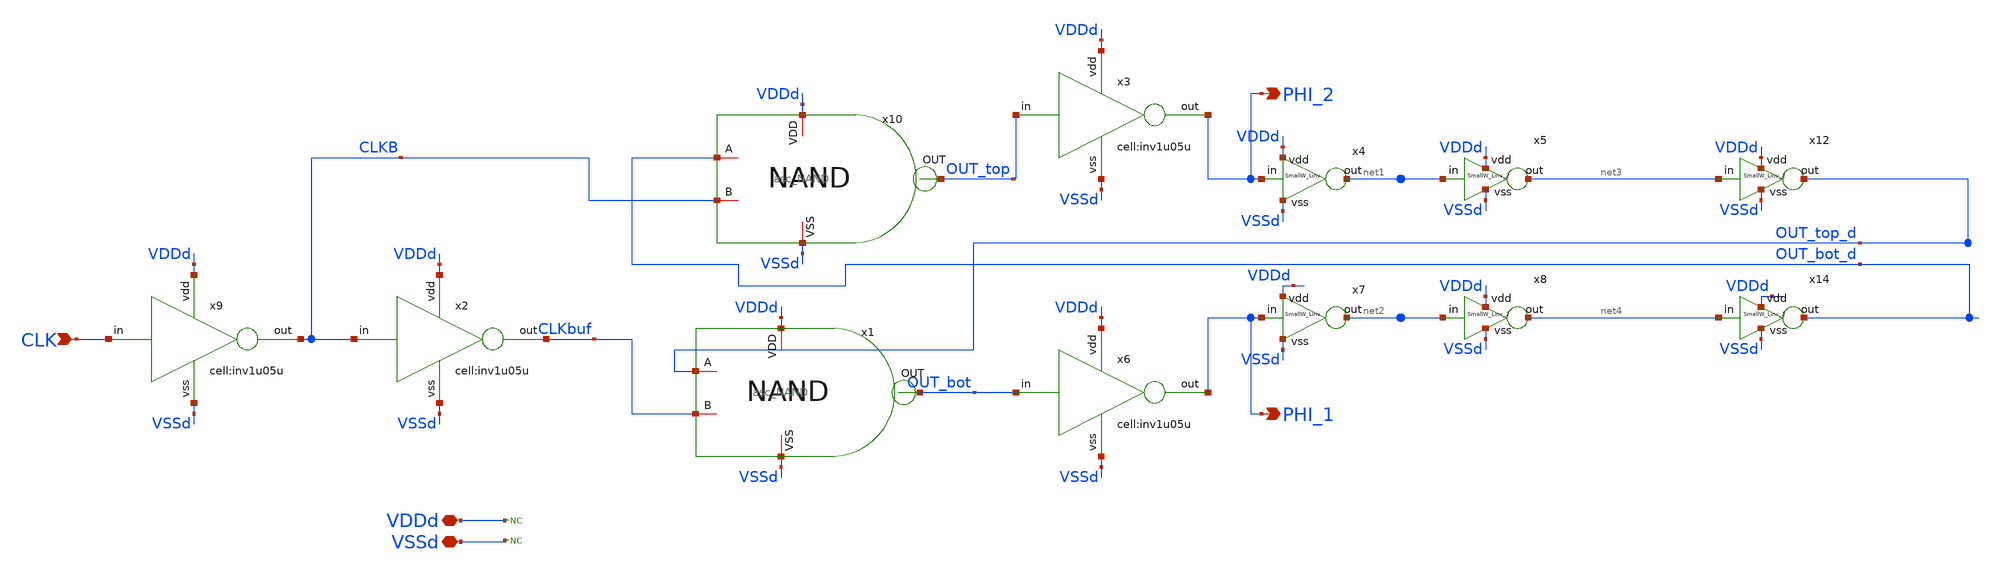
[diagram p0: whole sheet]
** sch_path: designs/libs/core_analog/qw_NOLclk/qw_NOLclk.sch
**.subckt qw_NOLclk CLK PHI_2 VDDd VSSd PHI_1
*.ipin CLK
*.opin PHI_2
*.iopin VDDd
*.iopin VSSd
*.opin PHI_1
* noconn VDDd
* noconn VSSd
x4 VDDd PHI_2 net1 VSSd SmallW_Linv
x7 VDDd PHI_1 net2 VSSd SmallW_Linv
x12 VDDd net3 OUT_top_d VSSd SmallW_Linv_2
x14 VDDd net4 OUT_bot_d VSSd SmallW_Linv_2
x5 VDDd net1 net3 VSSd SmallW_Linv_2
x8 VDDd net2 net4 VSSd SmallW_Linv_2
x9 CLK VDDd CLKB VSSd inv1u05u
x2 CLKB VDDd CLKbuf VSSd inv1u05u
x10 VDDd OUT_top OUT_bot_d CLKB VSSd asc_NAND
x1 VDDd OUT_bot OUT_top_d CLKbuf VSSd asc_NAND
x3 OUT_top VDDd PHI_2 VSSd inv1u05u
x6 OUT_bot VDDd PHI_1 VSSd inv1u05u
**.ends
.end
